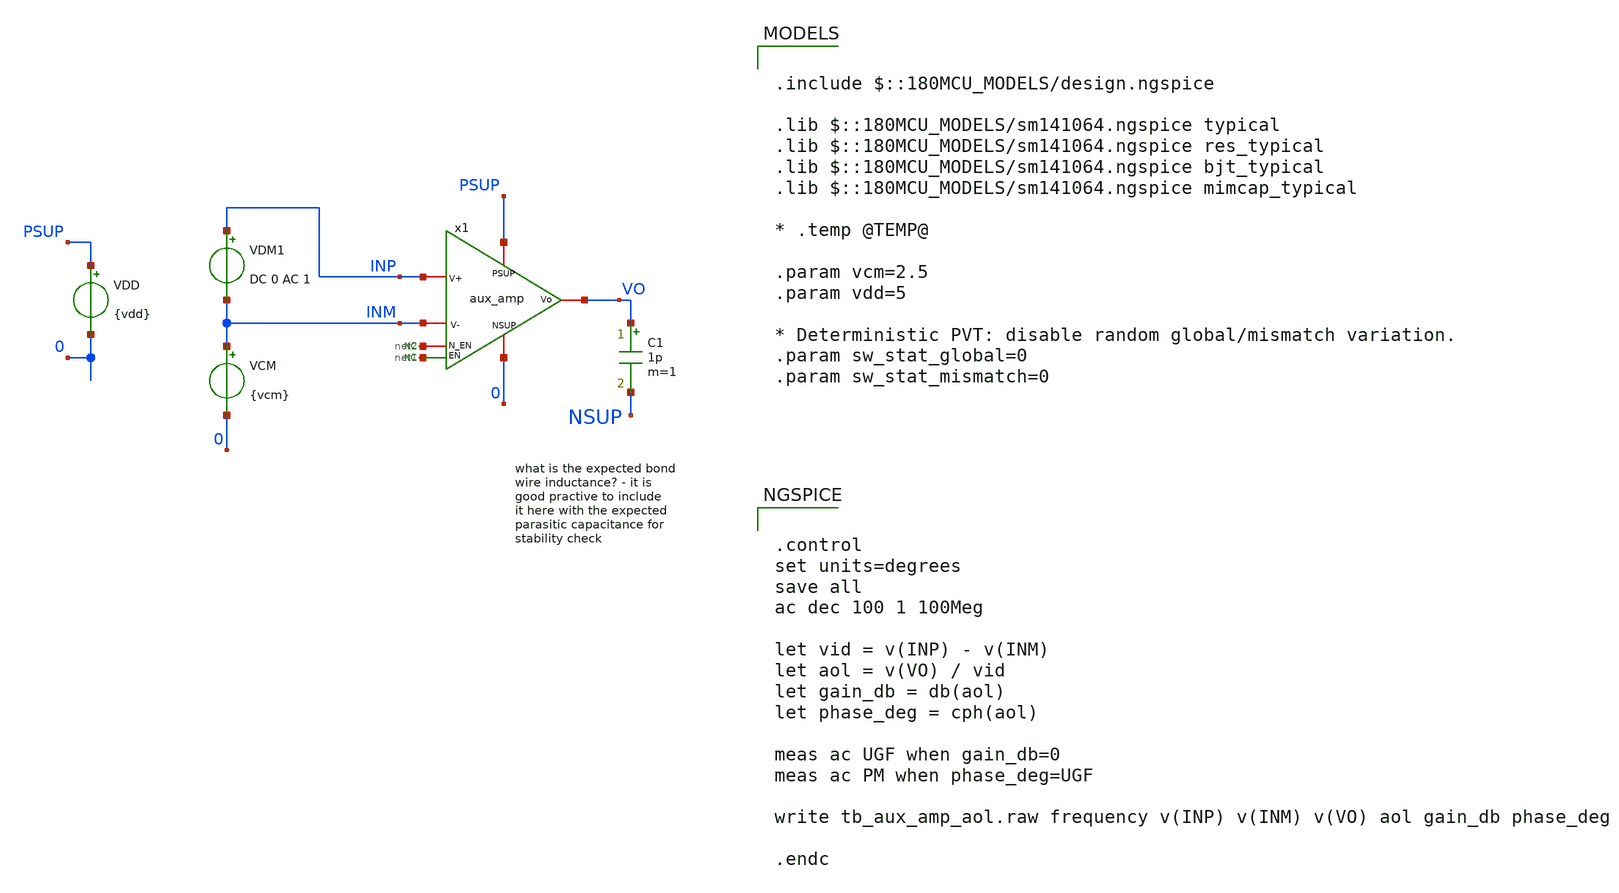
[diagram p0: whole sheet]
** sch_path: xschem/blocks/aux_amp_gb/tb_aux_amp_gb_aol.sch
**.subckt tb_aux_amp_gb_aol
VDD PSUP 0 {vdd}
VCM INM 0 {vcm}
* noconn #net1
* noconn #net2
VDM1 INP INM DC 0 AC 1
x1 PSUP VO INP INM net2 0 net1 aux_amp
C1 VO NSUP 1p m=1
**** begin user architecture code

.include $::180MCU_MODELS/design.ngspice

.lib $::180MCU_MODELS/sm141064.ngspice typical
.lib $::180MCU_MODELS/sm141064.ngspice res_typical
.lib $::180MCU_MODELS/sm141064.ngspice bjt_typical
.lib $::180MCU_MODELS/sm141064.ngspice mimcap_typical

* .temp @TEMP@

.param vcm=2.5
.param vdd=5

* Deterministic PVT: disable random global/mismatch variation.
.param sw_stat_global=0
.param sw_stat_mismatch=0



.control
set units=degrees
save all
ac dec 100 1 100Meg

let vid = v(INP) - v(INM)
let aol = v(VO) / vid
let gain_db = db(aol)
let phase_deg = cph(aol)

meas ac UGF when gain_db=0
meas ac PM when phase_deg=UGF

write tb_aux_amp_aol.raw frequency v(INP) v(INM) v(VO) aol gain_db phase_deg

.endc


**** end user architecture code
**.ends

* expanding   symbol:  blocks/aux_amp/aux_amp.sym # of pins=7
** sym_path: xschem/lib/aux_amp.sym
** sch_path: xschem/lib/aux_amp.sch
.subckt aux_amp PSUP Vo V+ V- N_EN NSUP EN
*.ipin PSUP
*.ipin NSUP
*.ipin N_EN
*.ipin EN
*.ipin V+
*.ipin V-
*.opin Vo
XM1 Vo V- net2 net2 nfet_06v0 L=1.80u W=0.80u nf=1 ad='int((nf+1)/2) * W/nf * 0.18u' as='int((nf+2)/2) * W/nf * 0.18u'
+ pd='2*int((nf+1)/2) * (W/nf + 0.18u)' ps='2*int((nf+2)/2) * (W/nf + 0.18u)' nrd='0.18u / W' nrs='0.18u / W'
+ sa=0 sb=0 sd=0 m=1
XM2 net1 V+ net2 net2 nfet_06v0 L=1.80u W=0.80u nf=1 ad='int((nf+1)/2) * W/nf * 0.18u' as='int((nf+2)/2) * W/nf * 0.18u'
+ pd='2*int((nf+1)/2) * (W/nf + 0.18u)' ps='2*int((nf+2)/2) * (W/nf + 0.18u)' nrd='0.18u / W' nrs='0.18u / W'
+ sa=0 sb=0 sd=0 m=1
XM5 net1 net1 PSUP PSUP pfet_06v0 L=0.55u W=0.30u nf=1 ad='int((nf+1)/2) * W/nf * 0.18u' as='int((nf+2)/2) * W/nf * 0.18u'
+ pd='2*int((nf+1)/2) * (W/nf + 0.18u)' ps='2*int((nf+2)/2) * (W/nf + 0.18u)' nrd='0.18u / W' nrs='0.18u / W'
+ sa=0 sb=0 sd=0 m=1
XM6 Vo net1 PSUP PSUP pfet_06v0 L=0.55u W=0.30u nf=1 ad='int((nf+1)/2) * W/nf * 0.18u' as='int((nf+2)/2) * W/nf * 0.18u'
+ pd='2*int((nf+1)/2) * (W/nf + 0.18u)' ps='2*int((nf+2)/2) * (W/nf + 0.18u)' nrd='0.18u / W' nrs='0.18u / W'
+ sa=0 sb=0 sd=0 m=1
I0 net2 NSUP 5u
* noconn N_EN
* noconn EN
.ends

.end
